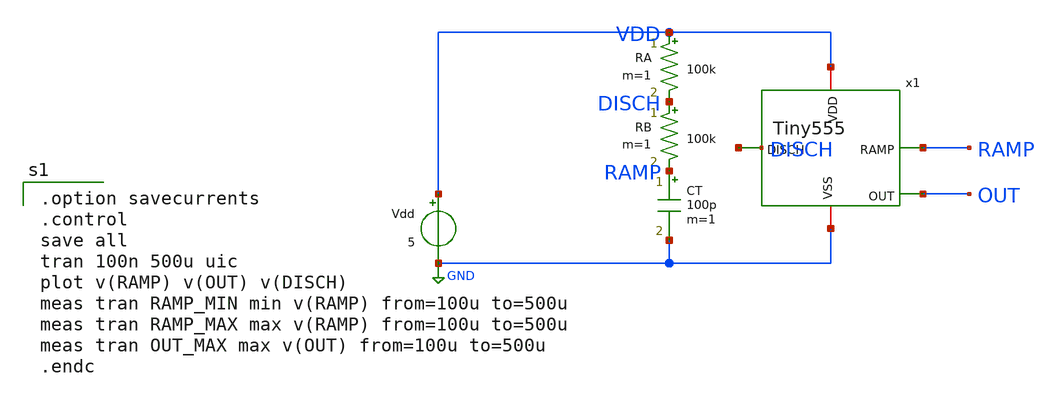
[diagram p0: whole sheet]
** sch_path: member_project/Tiny555/yamada3/xschem/tb_Tiny555_tran.sch
**.subckt tb_Tiny555_tran
Vdd VDD GND 5
x1 VDD RAMP OUT DISCH GND Tiny555
RA VDD DISCH 100k m=1
RB DISCH RAMP 100k m=1
CT RAMP GND 100p m=1
**** begin user architecture code
 .include $::LIB/ip62_models

.option savecurrents
.control
save all
tran 100n 500u uic
plot v(RAMP) v(OUT) v(DISCH)
meas tran RAMP_MIN min v(RAMP) from=100u to=500u
meas tran RAMP_MAX max v(RAMP) from=100u to=500u
meas tran OUT_MAX max v(OUT) from=100u to=500u
.endc

**** end user architecture code
**.ends
.GLOBAL GND
.end
